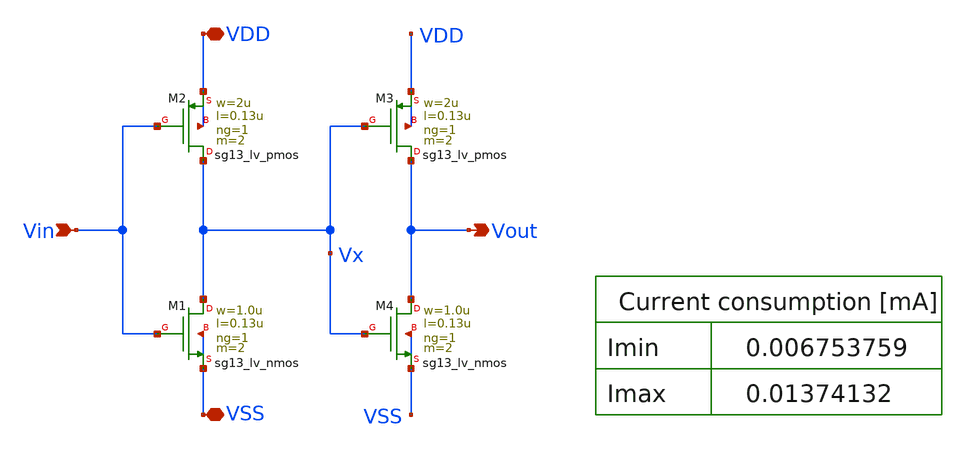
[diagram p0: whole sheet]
** sch_path: work/threshold_circuit/xschem/threshold_comparator.sch
**.subckt threshold_comparator VDD VSS Vin Vout
*.iopin VDD
*.iopin VSS
*.ipin Vin
*.opin Vout
XM2 Vx Vin VDD VDD sg13_lv_pmos w=2u l=0.13u ng=1 m=2 mm_ok=1
XM1 Vx Vin VSS VSS sg13_lv_nmos w=1.0u l=0.13u ng=1 m=2 mm_ok=1
XM3 Vout Vx VDD VDD sg13_lv_pmos w=2u l=0.13u ng=1 m=2 mm_ok=1
XM4 Vout Vx VSS VSS sg13_lv_nmos w=1.0u l=0.13u ng=1 m=2 mm_ok=1
**.ends
.end
